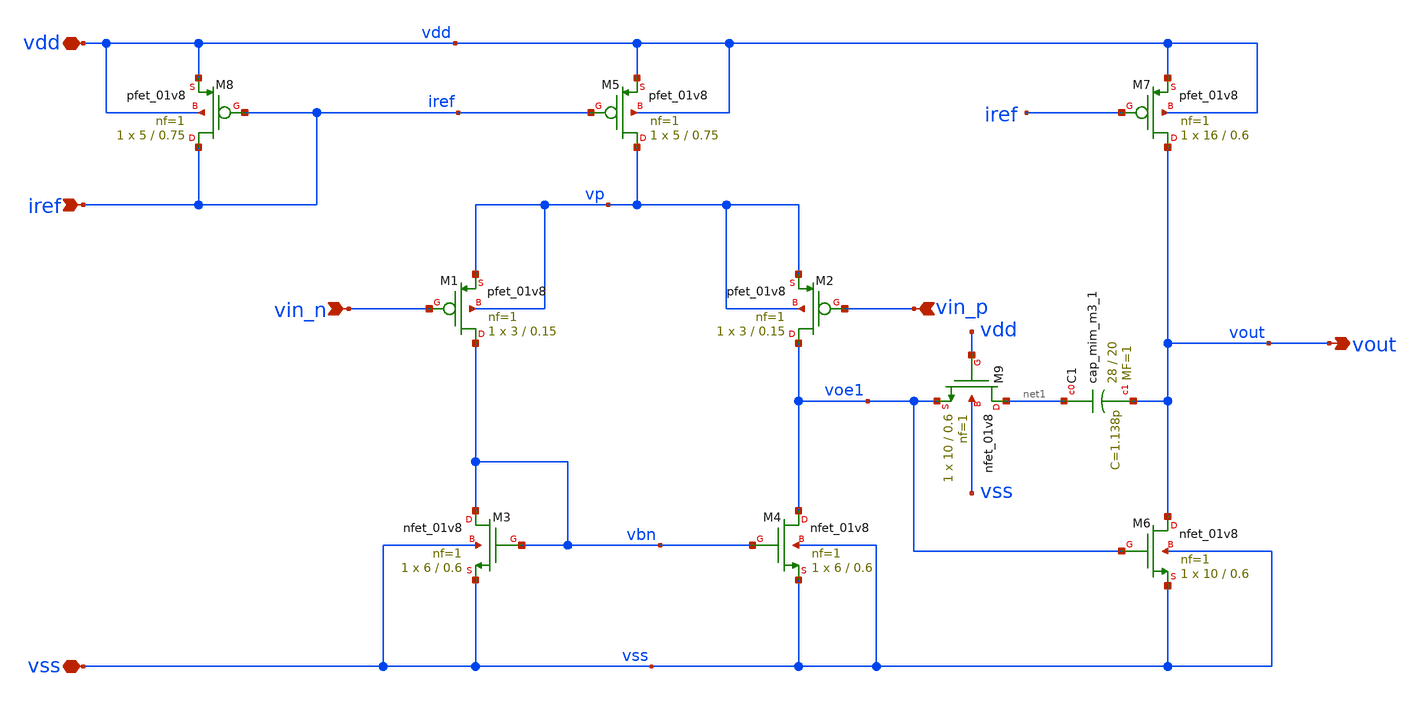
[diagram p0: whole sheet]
** sch_path: xschem/j_opamp.sch
**.subckt j_opamp vdd vss vin_n vin_p iref vout
*.iopin vdd
*.iopin vss
*.ipin vin_n
*.ipin vin_p
*.ipin iref
*.opin vout
XM1 vbn vin_n vp vp sky130_fd_pr__pfet_01v8 L=0.15 W=3 nf=1 ad='W * 0.29' as='W * 0.29' pd='2 * (W + 0.29)'
+ ps='2 * (W + 0.29)' nrd='0.29 / W' nrs='0.29 / W' sa=0 sb=0 sd=0 mult=1 m=1
XM2 voe1 vin_p vp vp sky130_fd_pr__pfet_01v8 L=0.15 W=3 nf=1 ad='W * 0.29' as='W * 0.29' pd='2 * (W + 0.29)'
+ ps='2 * (W + 0.29)' nrd='0.29 / W' nrs='0.29 / W' sa=0 sb=0 sd=0 mult=1 m=1
XM3 vbn vbn vss vss sky130_fd_pr__nfet_01v8 L=0.6 W=6 nf=1 ad='W * 0.29' as='W * 0.29' pd='2 * (W + 0.29)'
+ ps='2 * (W + 0.29)' nrd='0.29 / W' nrs='0.29 / W' sa=0 sb=0 sd=0 mult=1 m=1
XM4 voe1 vbn vss vss sky130_fd_pr__nfet_01v8 L=0.6 W=6 nf=1 ad='W * 0.29' as='W * 0.29' pd='2 * (W + 0.29)'
+ ps='2 * (W + 0.29)' nrd='0.29 / W' nrs='0.29 / W' sa=0 sb=0 sd=0 mult=1 m=1
XM5 vp iref vdd vdd sky130_fd_pr__pfet_01v8 L=0.75 W=5 nf=1 ad='W * 0.29' as='W * 0.29' pd='2 * (W + 0.29)'
+ ps='2 * (W + 0.29)' nrd='0.29 / W' nrs='0.29 / W' sa=0 sb=0 sd=0 mult=1 m=1
XM7 vout iref vdd vdd sky130_fd_pr__pfet_01v8 L=0.6 W=16 nf=1 ad='W * 0.29' as='W * 0.29' pd='2 * (W + 0.29)'
+ ps='2 * (W + 0.29)' nrd='0.29 / W' nrs='0.29 / W' sa=0 sb=0 sd=0 mult=1 m=1
XM8 iref iref vdd vdd sky130_fd_pr__pfet_01v8 L=0.75 W=5 nf=1 ad='W * 0.29' as='W * 0.29' pd='2 * (W + 0.29)'
+ ps='2 * (W + 0.29)' nrd='0.29 / W' nrs='0.29 / W' sa=0 sb=0 sd=0 mult=1 m=1
XM9 net1 vdd voe1 vss sky130_fd_pr__nfet_01v8 L=0.6 W=10 nf=1 ad='W * 0.29' as='W * 0.29' pd='2 * (W + 0.29)'
+ ps='2 * (W + 0.29)' nrd='0.29 / W' nrs='0.29 / W' sa=0 sb=0 sd=0 mult=1 m=1
XC1 net1 vout sky130_fd_pr__cap_mim_m3_1 W=28 L=20 MF=1 m=1
XM6 vout voe1 vss vss sky130_fd_pr__nfet_01v8 L=0.6 W=10 nf=1 ad='W * 0.29' as='W * 0.29' pd='2 * (W + 0.29)'
+ ps='2 * (W + 0.29)' nrd='0.29 / W' nrs='0.29 / W' sa=0 sb=0 sd=0 mult=1 m=1
**.ends
.end
